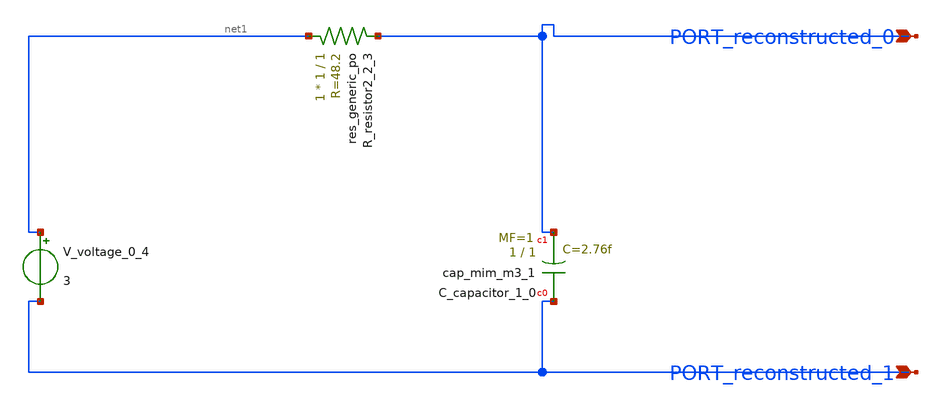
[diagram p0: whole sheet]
** sch_path: schematics/AMSNet/428.sch
**.subckt 428 PORT_reconstructed_1 PORT_reconstructed_0
*.ipin PORT_reconstructed_1
*.ipin PORT_reconstructed_0
XC_capacitor_1_0 PORT_reconstructed_1 PORT_reconstructed_0 sky130_fd_pr__cap_mim_m3_1 W=1 L=1 MF=1
+ m=1
XR_resistor2_2_3 net1 PORT_reconstructed_0 sky130_fd_pr__res_generic_po W=1 L=1 m=1
V_voltage_0_4 net1 PORT_reconstructed_1 3
**.ends
.end
